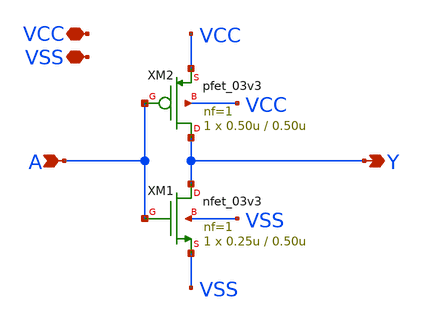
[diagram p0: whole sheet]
** sch_path: xschem/inverter.sch
**.subckt inverter VCC VSS A Y
*.iopin VCC
*.iopin VSS
*.ipin A
*.opin Y
XM1 Y A VSS VSS nfet_03v3 L=0.50u W=0.25u nf=1 ad='int((nf+1)/2) * W/nf * 0.18u' as='int((nf+2)/2) * W/nf * 0.18u'
+ pd='2*int((nf+1)/2) * (W/nf + 0.18u)' ps='2*int((nf+2)/2) * (W/nf + 0.18u)' nrd='0.18u / W' nrs='0.18u / W'
+ sa=0 sb=0 sd=0 m=1
XM2 Y A VCC VCC pfet_03v3 L=0.50u W=0.50u nf=1 ad='int((nf+1)/2) * W/nf * 0.18u' as='int((nf+2)/2) * W/nf * 0.18u'
+ pd='2*int((nf+1)/2) * (W/nf + 0.18u)' ps='2*int((nf+2)/2) * (W/nf + 0.18u)' nrd='0.18u / W' nrs='0.18u / W'
+ sa=0 sb=0 sd=0 m=1
**.ends
.end
